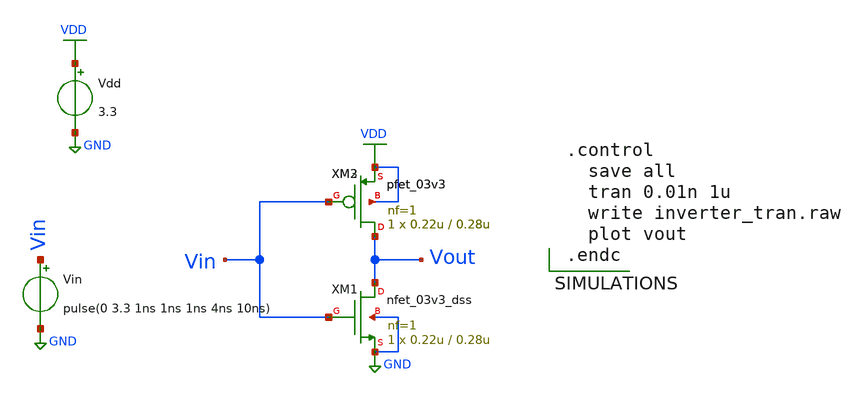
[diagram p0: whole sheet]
** sch_path: OR/inverter_tran.sch
**.subckt inverter_tran
XM1 Vout Vin GND GND nfet_03v3_dss L=0.28u W=0.22u nf=1 ad='int((nf+1)/2) * W/nf * 0.18u' as='int((nf+2)/2) * W/nf * 0.18u'
+ pd='2*int((nf+1)/2) * (W/nf + 0.18u)' ps='2*int((nf+2)/2) * (W/nf + 0.18u)' nrd='0.18u / W' nrs='0.18u / W'
+ sa=0 sb=0 sd=0 m=1
XM2 Vout Vin VDD VDD pfet_03v3 L=0.28u W=0.22u nf=1 ad='int((nf+1)/2) * W/nf * 0.18u' as='int((nf+2)/2) * W/nf * 0.18u'
+ pd='2*int((nf+1)/2) * (W/nf + 0.18u)' ps='2*int((nf+2)/2) * (W/nf + 0.18u)' nrd='0.18u / W' nrs='0.18u / W'
+ sa=0 sb=0 sd=0 m=1
Vdd VDD GND 3.3
Vin Vin GND pulse(0 3.3 1ns 1ns 1ns 4ns 10ns)
XM3 Vout Vin VDD VDD pfet_03v3 L=0.28u W=0.22u nf=1 ad='int((nf+1)/2) * W/nf * 0.18u' as='int((nf+2)/2) * W/nf * 0.18u'
+ pd='2*int((nf+1)/2) * (W/nf + 0.18u)' ps='2*int((nf+2)/2) * (W/nf + 0.18u)' nrd='0.18u / W' nrs='0.18u / W'
+ sa=0 sb=0 sd=0 m=1
**** begin user architecture code


.control
  save all
  tran 0.01n 1u
  write inverter_tran.raw
  plot vout
.endc




.include /foss/pdks/gf180mcuD/libs.tech/ngspice/design.ngspice
.lib /foss/pdks/gf180mcuD/libs.tech/ngspice/sm141064.ngspice typical


**** end user architecture code
**.ends
.GLOBAL VDD
.GLOBAL GND
.end
